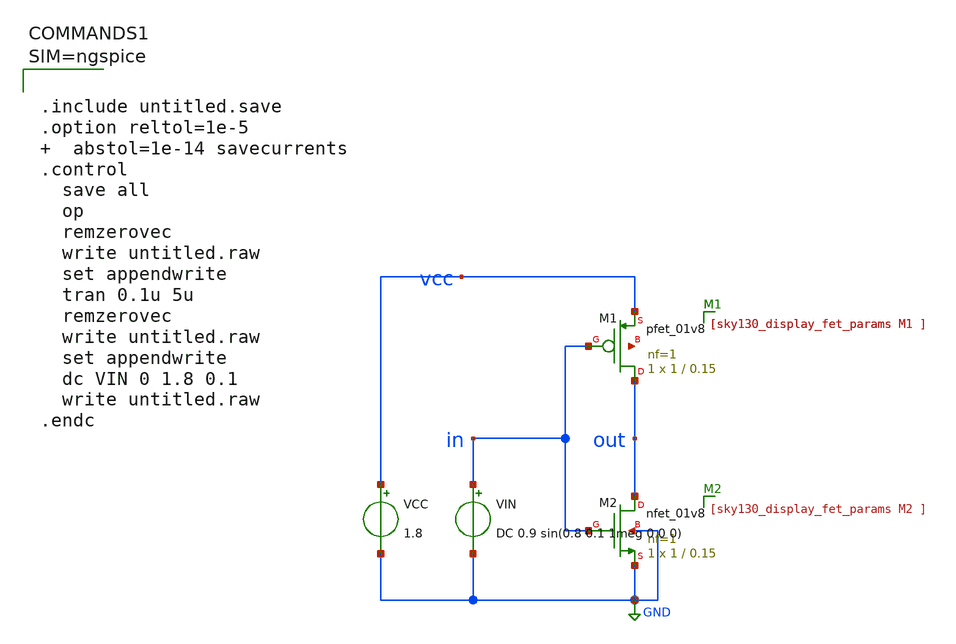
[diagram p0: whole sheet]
** sch_path: untitled.sch
**.subckt untitled
XM2 out in GND GND sky130_fd_pr__nfet_01v8 L=0.15 W=1 nf=1 ad='int((1 + 1)/2) * 1 / 1 * 0.29' as='int((1 + 2)/2) * 1 / 1 * 0.29'
+ pd='2*int((1 + 1)/2) * (1 / 1 + 0.29)' ps='2*int((1 + 2)/2) * (1 / 1 + 0.29)' nrd='0.29 / 1 ' nrs='0.29 / 1 '
+ sa=0 sb=0 sd=0 mult=1 m=1
XM1 out in vcc net1 sky130_fd_pr__pfet_01v8 L=0.15 W=1 nf=1 ad='int((nf+1)/2) * W/nf * 0.29' as='int((nf+2)/2) * W/nf * 0.29'
+ pd='2*int((nf+1)/2) * (W/nf + 0.29)' ps='2*int((nf+2)/2) * (W/nf + 0.29)' nrd='0.29 / W' nrs='0.29 / W'
+ sa=0 sb=0 sd=0 mult=1 m=1
VIN in GND DC 0.9 sin(0.8 0.1 1meg 0 0 0)
.save i(vin)
VCC vcc GND 1.8
.save i(vcc)
**** begin user architecture code

** opencircuitdesign pdks install
.lib $::SKYWATER_MODELS/sky130.lib.spice tt




.include untitled.save
.option reltol=1e-5   abstol=1e-14 savecurrents
.control
  save all
  op
  remzerovec
  write untitled.raw
  set appendwrite
  tran 0.1u 5u
  remzerovec
  write untitled.raw
  set appendwrite
  dc VIN 0 1.8 0.1
  write untitled.raw
.endc



**** end user architecture code
**.ends
.GLOBAL GND
.end
